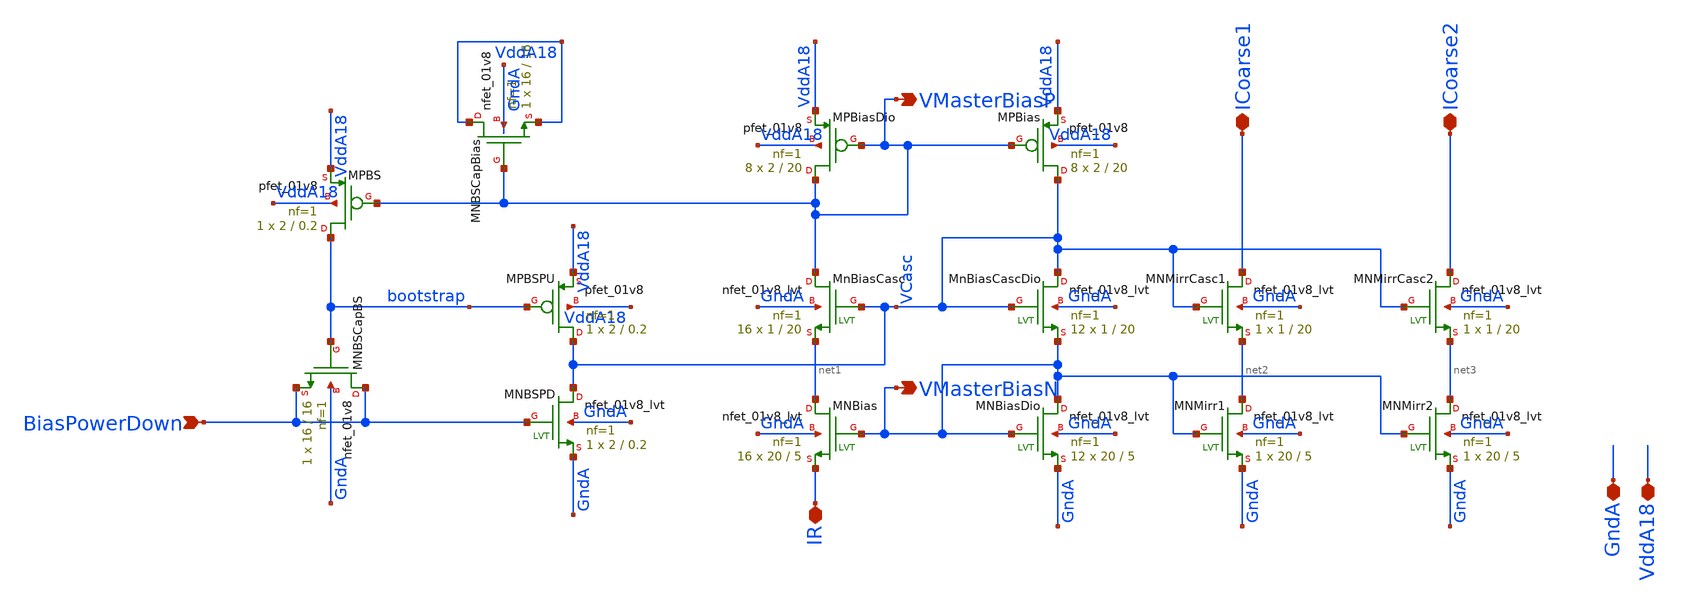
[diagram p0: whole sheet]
** sch_path: analog/xschem/BiasMasterBias.sch
**.subckt BiasMasterBias VMasterBiasP IR VddA18 GndA VMasterBiasN ICoarse1 ICoarse2 BiasPowerDown
*.opin VMasterBiasP
*.iopin IR
*.iopin VddA18
*.iopin GndA
*.opin VMasterBiasN
*.iopin ICoarse1
*.iopin ICoarse2
*.ipin BiasPowerDown
XMNBiasDio VMasterBiasN VMasterBiasN GndA GndA sky130_fd_pr__nfet_01v8_lvt L=5 W=20 nf=1 ad='int((1 + 1)/2) * 20 / 1 * 0.29'
+ as='int((1 + 2)/2) * 20 / 1 * 0.29' pd='2*int((1 + 1)/2) * (20 / 1 + 0.29)' ps='2*int((1 + 2)/2) * (20 / 1 + 0.29)'
+ nrd='0.29 / 20 ' nrs='0.29 / 20 ' sa=0 sb=0 sd=0 mult=12 m=12
XMPBias VCasc VMasterBiasP VddA18 VddA18 sky130_fd_pr__pfet_01v8 L=20 W=2 nf=1 ad='int((1 + 1)/2) * 2 / 1 * 0.29'
+ as='int((1 + 2)/2) * 2 / 1 * 0.29' pd='2*int((1 + 1)/2) * (2 / 1 + 0.29)' ps='2*int((1 + 2)/2) * (2 / 1 + 0.29)'
+ nrd='0.29 / 2 ' nrs='0.29 / 2 ' sa=0 sb=0 sd=0 mult=8 m=8
XMNBias net1 VMasterBiasN IR GndA sky130_fd_pr__nfet_01v8_lvt L=5 W=20 nf=1 ad='int((1 + 1)/2) * 20 / 1 * 0.29'
+ as='int((1 + 2)/2) * 20 / 1 * 0.29' pd='2*int((1 + 1)/2) * (20 / 1 + 0.29)' ps='2*int((1 + 2)/2) * (20 / 1 + 0.29)'
+ nrd='0.29 / 20 ' nrs='0.29 / 20 ' sa=0 sb=0 sd=0 mult=16 m=16
XMnBiasCascDio VCasc VCasc VMasterBiasN GndA sky130_fd_pr__nfet_01v8_lvt L=20 W=1 nf=1 ad='int((1 + 1)/2) * 1 / 1 * 0.29'
+ as='int((1 + 2)/2) * 1 / 1 * 0.29' pd='2*int((1 + 1)/2) * (1 / 1 + 0.29)' ps='2*int((1 + 2)/2) * (1 / 1 + 0.29)'
+ nrd='0.29 / 1 ' nrs='0.29 / 1 ' sa=0 sb=0 sd=0 mult=12 m=12
XMnBiasCasc VMasterBiasP VCasc net1 GndA sky130_fd_pr__nfet_01v8_lvt L=20 W=1 nf=1 ad='int((1 + 1)/2) * 1 / 1 * 0.29'
+ as='int((1 + 2)/2) * 1 / 1 * 0.29' pd='2*int((1 + 1)/2) * (1 / 1 + 0.29)' ps='2*int((1 + 2)/2) * (1 / 1 + 0.29)'
+ nrd='0.29 / 1 ' nrs='0.29 / 1 ' sa=0 sb=0 sd=0 mult=16 m=16
XMPBiasDio VMasterBiasP VMasterBiasP VddA18 VddA18 sky130_fd_pr__pfet_01v8 L=20 W=2 nf=1 ad='int((1 + 1)/2) * 2 / 1 * 0.29'
+ as='int((1 + 2)/2) * 2 / 1 * 0.29' pd='2*int((1 + 1)/2) * (2 / 1 + 0.29)' ps='2*int((1 + 2)/2) * (2 / 1 + 0.29)'
+ nrd='0.29 / 2 ' nrs='0.29 / 2 ' sa=0 sb=0 sd=0 mult=8 m=8
XMNMirr1 net2 VMasterBiasN GndA GndA sky130_fd_pr__nfet_01v8_lvt L=5 W=20 nf=1 ad='int((1 + 1)/2) * 20 / 1 * 0.29'
+ as='int((1 + 2)/2) * 20 / 1 * 0.29' pd='2*int((1 + 1)/2) * (20 / 1 + 0.29)' ps='2*int((1 + 2)/2) * (20 / 1 + 0.29)'
+ nrd='0.29 / 20 ' nrs='0.29 / 20 ' sa=0 sb=0 sd=0 mult=1 m=1
XMNMirrCasc1 ICoarse1 VCasc net2 GndA sky130_fd_pr__nfet_01v8_lvt L=20 W=1 nf=1 ad='int((1 + 1)/2) * 1 / 1 * 0.29'
+ as='int((1 + 2)/2) * 1 / 1 * 0.29' pd='2*int((1 + 1)/2) * (1 / 1 + 0.29)' ps='2*int((1 + 2)/2) * (1 / 1 + 0.29)'
+ nrd='0.29 / 1 ' nrs='0.29 / 1 ' sa=0 sb=0 sd=0 mult=1 m=1
XMNMirr2 net3 VMasterBiasN GndA GndA sky130_fd_pr__nfet_01v8_lvt L=5 W=20 nf=1 ad='int((1 + 1)/2) * 20 / 1 * 0.29'
+ as='int((1 + 2)/2) * 20 / 1 * 0.29' pd='2*int((1 + 1)/2) * (20 / 1 + 0.29)' ps='2*int((1 + 2)/2) * (20 / 1 + 0.29)'
+ nrd='0.29 / 20 ' nrs='0.29 / 20 ' sa=0 sb=0 sd=0 mult=1 m=1
XMNMirrCasc2 ICoarse2 VCasc net3 GndA sky130_fd_pr__nfet_01v8_lvt L=20 W=1 nf=1 ad='int((1 + 1)/2) * 1 / 1 * 0.29'
+ as='int((1 + 2)/2) * 1 / 1 * 0.29' pd='2*int((1 + 1)/2) * (1 / 1 + 0.29)' ps='2*int((1 + 2)/2) * (1 / 1 + 0.29)'
+ nrd='0.29 / 1 ' nrs='0.29 / 1 ' sa=0 sb=0 sd=0 mult=1 m=1
XMNBSPD VCasc BiasPowerDown GndA GndA sky130_fd_pr__nfet_01v8_lvt L=0.2 W=2 nf=1 ad='int((1 + 1)/2) * 2 / 1 * 0.29'
+ as='int((1 + 2)/2) * 2 / 1 * 0.29' pd='2*int((1 + 1)/2) * (2 / 1 + 0.29)' ps='2*int((1 + 2)/2) * (2 / 1 + 0.29)'
+ nrd='0.29 / 2 ' nrs='0.29 / 2 ' sa=0 sb=0 sd=0 mult=1 m=1
XMNBSCapBias VddA18 VMasterBiasP VddA18 GndA sky130_fd_pr__nfet_01v8 L=16 W=16 nf=1 ad='int((1 + 1)/2) * 16 / 1 * 0.29'
+ as='int((1 + 2)/2) * 16 / 1 * 0.29' pd='2*int((1 + 1)/2) * (16 / 1 + 0.29)' ps='2*int((1 + 2)/2) * (16 / 1 + 0.29)'
+ nrd='0.29 / 16 ' nrs='0.29 / 16 ' sa=0 sb=0 sd=0 mult=1 m=1
XMPBS bootstrap VMasterBiasP VddA18 VddA18 sky130_fd_pr__pfet_01v8 L=0.2 W=2 nf=1 ad='int((1 + 1)/2) * 2 / 1 * 0.29'
+ as='int((1 + 2)/2) * 2 / 1 * 0.29' pd='2*int((1 + 1)/2) * (2 / 1 + 0.29)' ps='2*int((1 + 2)/2) * (2 / 1 + 0.29)'
+ nrd='0.29 / 2 ' nrs='0.29 / 2 ' sa=0 sb=0 sd=0 mult=1 m=1
XMNBSCapBS BiasPowerDown bootstrap BiasPowerDown GndA sky130_fd_pr__nfet_01v8 L=16 W=16 nf=1 ad='int((1 + 1)/2) * 16 / 1 * 0.29'
+ as='int((1 + 2)/2) * 16 / 1 * 0.29' pd='2*int((1 + 1)/2) * (16 / 1 + 0.29)' ps='2*int((1 + 2)/2) * (16 / 1 + 0.29)'
+ nrd='0.29 / 16 ' nrs='0.29 / 16 ' sa=0 sb=0 sd=0 mult=1 m=1
XMPBSPU VCasc bootstrap VddA18 VddA18 sky130_fd_pr__pfet_01v8 L=0.2 W=2 nf=1 ad='int((1 + 1)/2) * 2 / 1 * 0.29'
+ as='int((1 + 2)/2) * 2 / 1 * 0.29' pd='2*int((1 + 1)/2) * (2 / 1 + 0.29)' ps='2*int((1 + 2)/2) * (2 / 1 + 0.29)'
+ nrd='0.29 / 2 ' nrs='0.29 / 2 ' sa=0 sb=0 sd=0 mult=1 m=1
**.ends
.end
